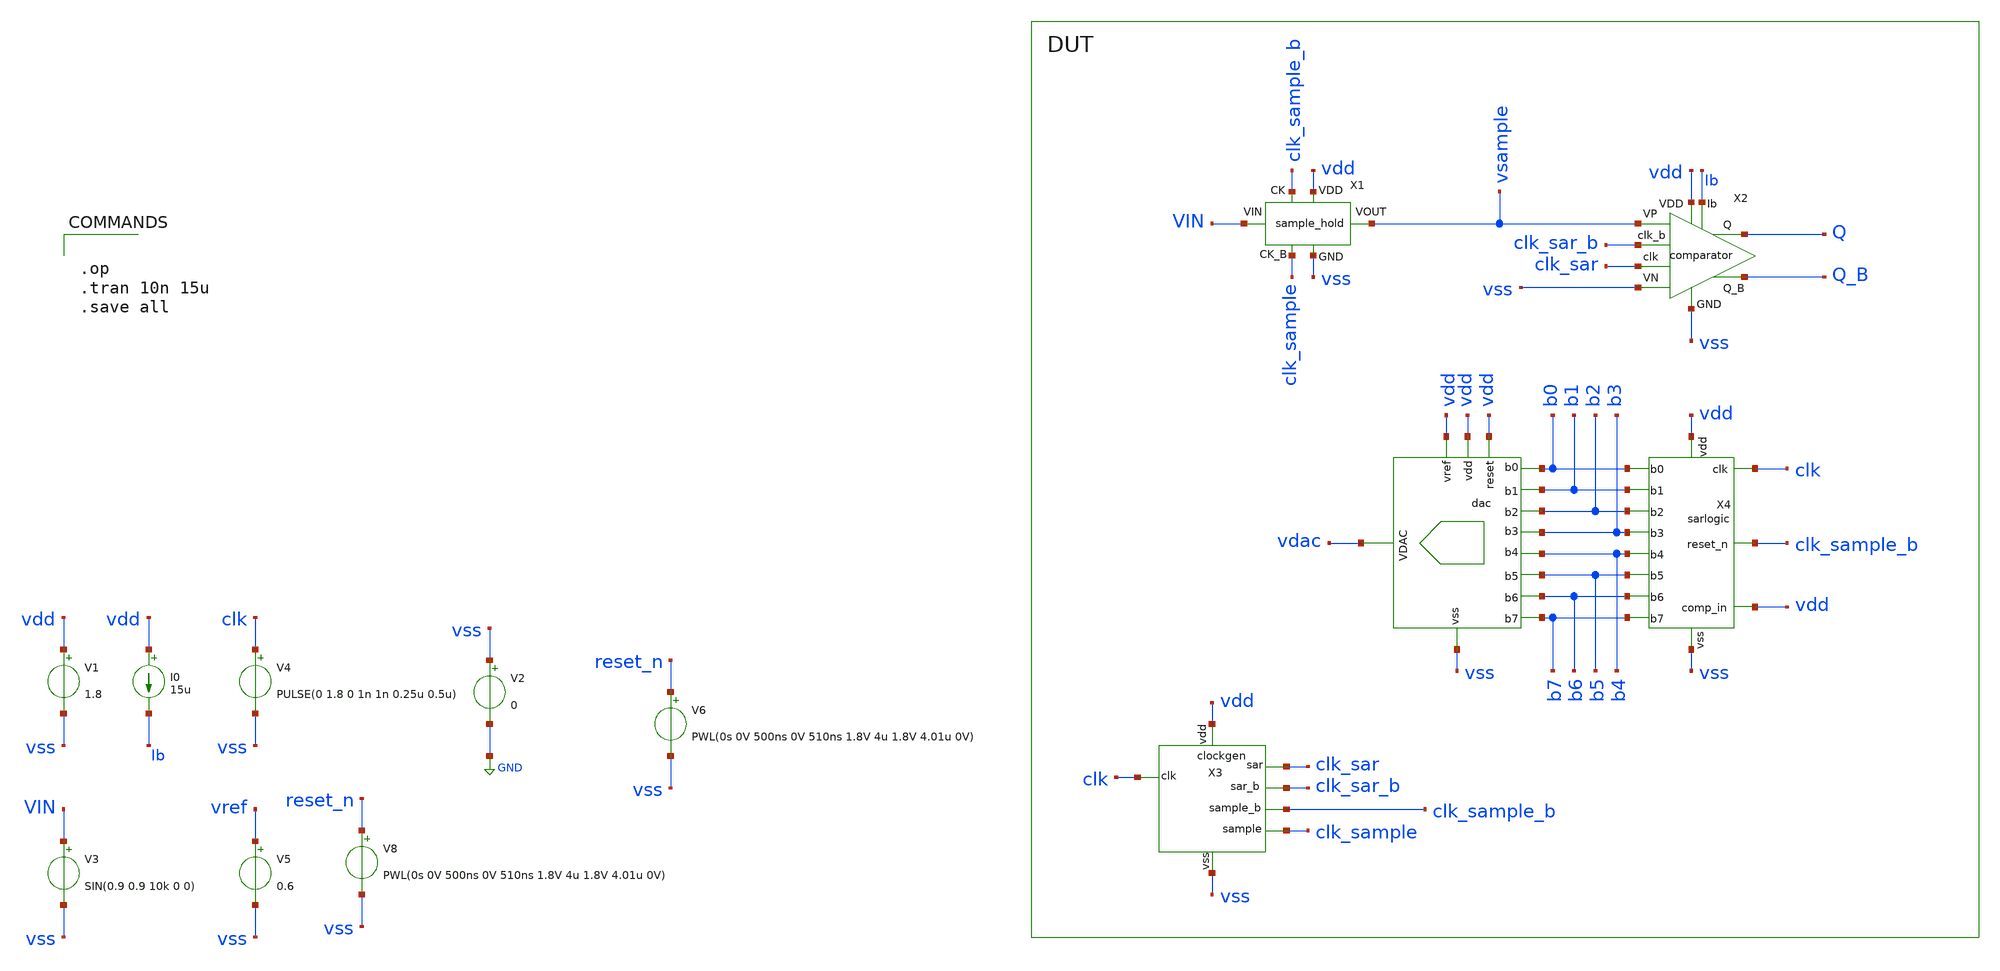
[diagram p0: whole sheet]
** sch_path: xschem/adc_top.sch
.lib $::SKYWATER_MODELS/sky130.lib.spice tt
.include $::SKYWATER_STDCELLS/sky130_fd_sc_hd.spice

**.subckt adc_top
V1 vdd vss 1.8
V3 VIN vss SIN(0.9 0.9 10k 0 0)
V4 clk vss PULSE(0 1.8 0 1n 1n 0.25u 0.5u)
I0 vdd Ib 15u
X2 vsample vss vss Q_B Q vdd clk_sar Ib clk_sar_b comparator
X1 vss vdd VIN vsample clk_sample_b clk_sample sample_hold
X3 clk vdd clk_sar clk_sample vss clk_sar_b clk_sample_b clockgen
V5 vref vss 0.6
X4 b0 b1 clk clk_sample_b vdd vdd vss b2 b3 b4 b5 b6 b7 sarlogic
X1 vss vdac vdd vdd b0 b1 b2 b3 b4 b5 b6 b7 vdd dac
V2 vss GND 0
V8 reset_n vss PWL(0s 0V 500ns 0V 510ns 1.8V 4u 1.8V 4.01u 0V)
V6 reset_n vss PWL(0s 0V 500ns 0V 510ns 1.8V 4u 1.8V 4.01u 0V)
**** begin user architecture code


.op
.tran 10n 15u
.save all


**** end user architecture code
**.ends
.GLOBAL GND
.end
